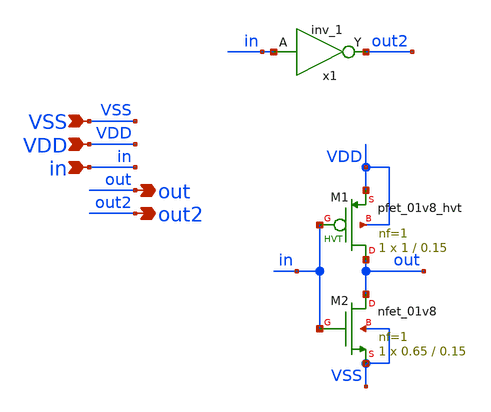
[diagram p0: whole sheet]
** sch_path: designs/inv_test.sch
**.subckt inv_test VDD in VSS out out2
*.ipin VDD
*.ipin in
*.ipin VSS
*.opin out
*.opin out2
XM2 out in VSS VSS sky130_fd_pr__nfet_01v8 L=0.15 W=0.65 nf=1 ad='int((nf+1)/2) * W/nf * 0.29' as='int((nf+2)/2) * W/nf * 0.29'
+ pd='2*int((nf+1)/2) * (W/nf + 0.29)' ps='2*int((nf+2)/2) * (W/nf + 0.29)' nrd='0.29 / W' nrs='0.29 / W'
+ sa=0 sb=0 sd=0 mult=1 m=1
XM1 out in VDD VDD sky130_fd_pr__pfet_01v8_hvt L=0.15 W=1 nf=1 ad='int((nf+1)/2) * W/nf * 0.29' as='int((nf+2)/2) * W/nf * 0.29'
+ pd='2*int((nf+1)/2) * (W/nf + 0.29)' ps='2*int((nf+2)/2) * (W/nf + 0.29)' nrd='0.29 / W' nrs='0.29 / W'
+ sa=0 sb=0 sd=0 mult=1 m=1
x1 in VSS VSS VDD VDD out2 sky130_fd_sc_hd__inv_1
**** begin user architecture code

.include $::SKYWATER_MODELS/cells/nfet_01v8/sky130_fd_pr__nfet_01v8__tt.corner.spice
.include $::SKYWATER_MODELS/cells/nfet_01v8_lvt/sky130_fd_pr__nfet_01v8_lvt__tt.corner.spice
.include $::SKYWATER_MODELS/cells/pfet_01v8/sky130_fd_pr__pfet_01v8__tt.corner.spice
.include $::SKYWATER_MODELS/cells/nfet_03v3_nvt/sky130_fd_pr__nfet_03v3_nvt__tt.corner.spice
.include $::SKYWATER_MODELS/cells/nfet_05v0_nvt/sky130_fd_pr__nfet_05v0_nvt__tt.corner.spice
.include $::SKYWATER_MODELS/cells/esd_nfet_01v8/sky130_fd_pr__esd_nfet_01v8__tt.corner.spice
.include $::SKYWATER_MODELS/cells/pfet_01v8_lvt/sky130_fd_pr__pfet_01v8_lvt__tt.corner.spice
.include $::SKYWATER_MODELS/cells/pfet_01v8_hvt/sky130_fd_pr__pfet_01v8_hvt__tt.corner.spice
.include $::SKYWATER_MODELS/cells/esd_pfet_g5v0d10v5/sky130_fd_pr__esd_pfet_g5v0d10v5__tt.corner.spice
.include $::SKYWATER_MODELS/cells/pfet_g5v0d10v5/sky130_fd_pr__pfet_g5v0d10v5__tt.corner.spice
.include $::SKYWATER_MODELS/cells/pfet_g5v0d16v0/sky130_fd_pr__pfet_g5v0d16v0__tt.corner.spice
.include $::SKYWATER_MODELS/cells/nfet_g5v0d10v5/sky130_fd_pr__nfet_g5v0d10v5__tt.corner.spice
.include $::SKYWATER_MODELS/cells/nfet_g5v0d16v0/sky130_fd_pr__nfet_g5v0d16v0__tt_discrete.corner.spice
.include $::SKYWATER_MODELS/cells/esd_nfet_g5v0d10v5/sky130_fd_pr__esd_nfet_g5v0d10v5__tt.corner.spice
.include $::SKYWATER_MODELS/models/corners/tt/nonfet.spice
* Standard cells
.include $::SKYWATER_STDCELLS/cells/inv/sky130_fd_sc_hd__inv_1.spice
* Mismatch parameters
.include $::SKYWATER_MODELS/cells/nfet_01v8/sky130_fd_pr__nfet_01v8__mismatch.corner.spice
.include $::SKYWATER_MODELS/cells/pfet_01v8/sky130_fd_pr__pfet_01v8__mismatch.corner.spice
.include $::SKYWATER_MODELS/cells/nfet_01v8_lvt/sky130_fd_pr__nfet_01v8_lvt__mismatch.corner.spice
.include $::SKYWATER_MODELS/cells/pfet_01v8_lvt/sky130_fd_pr__pfet_01v8_lvt__mismatch.corner.spice
.include $::SKYWATER_MODELS/cells/pfet_01v8_hvt/sky130_fd_pr__pfet_01v8_hvt__mismatch.corner.spice
.include $::SKYWATER_MODELS/cells/nfet_g5v0d10v5/sky130_fd_pr__nfet_g5v0d10v5__mismatch.corner.spice
.include $::SKYWATER_MODELS/cells/pfet_g5v0d10v5/sky130_fd_pr__pfet_g5v0d10v5__mismatch.corner.spice
.include $::SKYWATER_MODELS/cells/nfet_05v0_nvt/sky130_fd_pr__nfet_05v0_nvt__mismatch.corner.spice
.include $::SKYWATER_MODELS/cells/nfet_03v3_nvt/sky130_fd_pr__nfet_03v3_nvt__mismatch.corner.spice
* Resistor$::SKYWATER_MODELS/Capacitor
.include $::SKYWATER_MODELS/models/r+c/res_typical__cap_typical.spice
.include $::SKYWATER_MODELS/models/r+c/res_typical__cap_typical__lin.spice
* Special cells
.include $::SKYWATER_MODELS/models/corners/tt/specialized_cells.spice
* All models
.include $::SKYWATER_MODELS/models/all.spice
* Corner
.include $::SKYWATER_MODELS/models/corners/tt/rf.spice

**** end user architecture code
**.ends
**** begin user architecture code

.include inv_test_commands.spice

**** end user architecture code
.end
